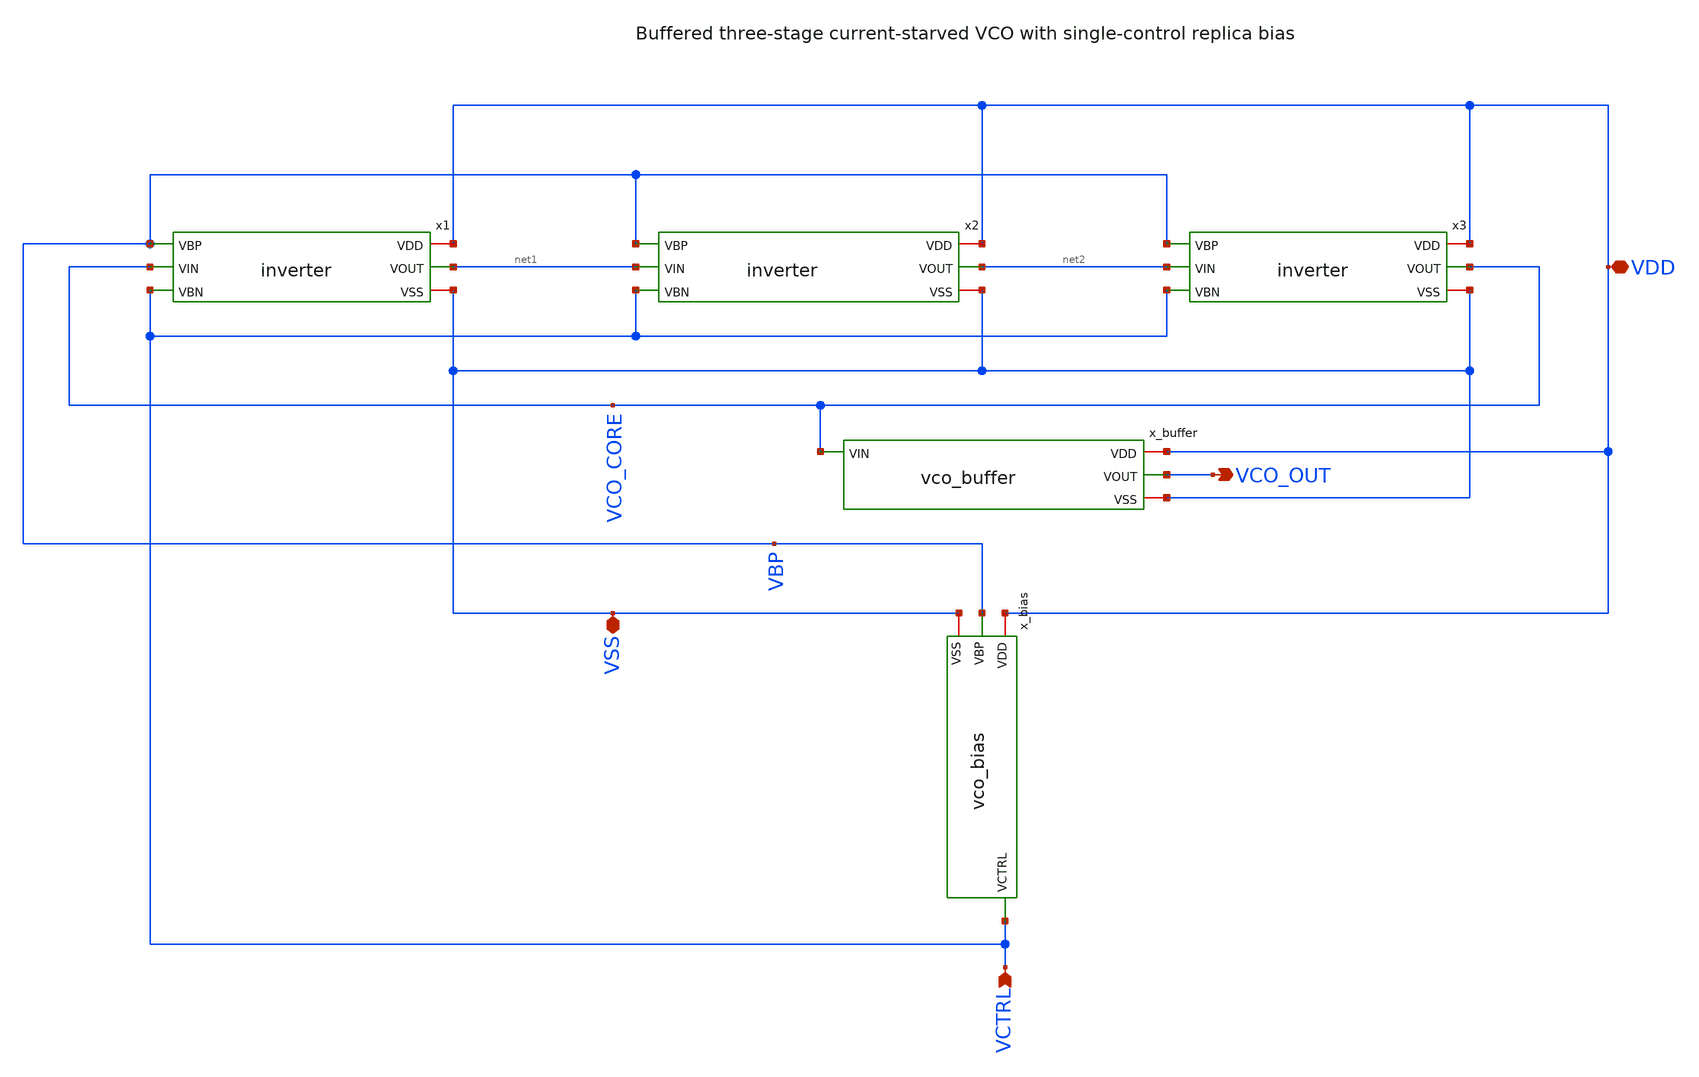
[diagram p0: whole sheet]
** sch_path: macros/pll_analog/schematic/xschem/ring_oscillator.sch
**.subckt ring_oscillator VCTRL VDD VSS VCO_OUT
*.ipin VCTRL
*.iopin VDD
*.iopin VSS
*.opin VCO_OUT
x1 VDD VBP VCO_CORE net1 VCTRL VSS inverter
x2 VDD VBP net1 net2 VCTRL VSS inverter
x3 VDD VBP net2 VCO_CORE VCTRL VSS inverter
x_bias VDD VBP VCTRL VSS vco_bias
x_buffer VDD VCO_CORE VCO_OUT VSS vco_buffer
**.ends
.end
